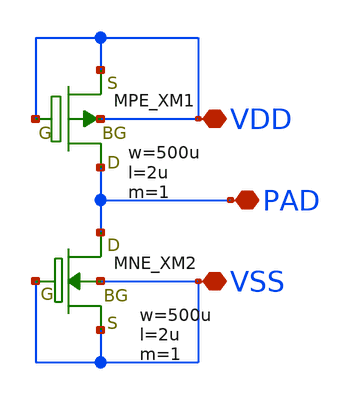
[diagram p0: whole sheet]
** sch_path: libs.tech/xschem/TR-1um_frame/OSS_ESD_5V_ANA.sch
**.subckt OSS_ESD_5V_ANA PAD VDD VSS
*.iopin PAD
*.iopin VDD
*.iopin VSS
XXM1 PAD VDD VDD VDD MPE w=500u l=2u as=0 ad=0 ps=0 pd=0 nrd=0 nrs=0 m=1
XXM2 PAD VSS VSS VSS MNE w=500u l=2u as=0 ad=0 ps=0 pd=0 nrd=0 nrs=0 m=1
**.ends
.end
